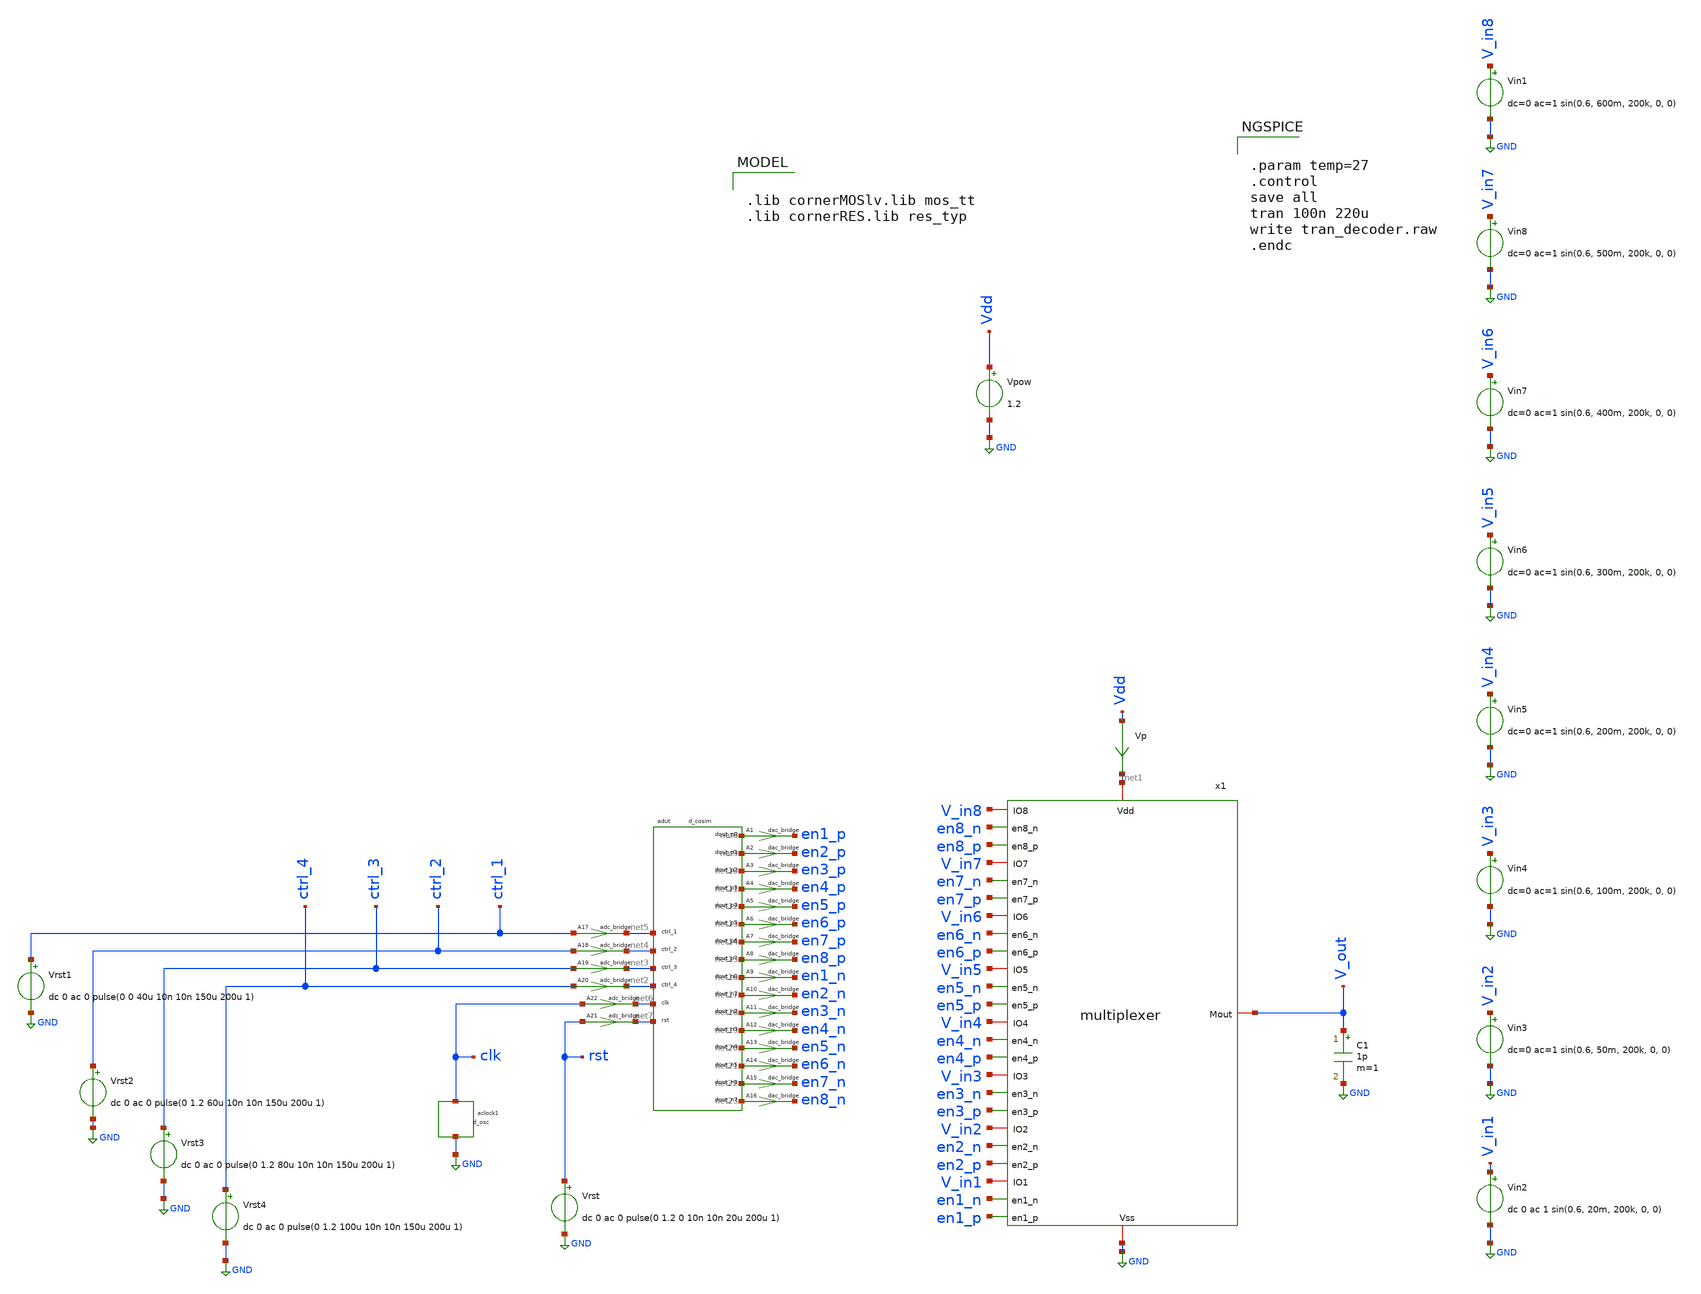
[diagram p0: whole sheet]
** sch_path: CHIPCHILE_CANELOS24_WorkshopTO/design_data/xschem/multiplexer/multiplexer_mixed_decoder_tb.sch
* Copyright 2023 IHP PDK Authors
**.subckt multiplexer_mixed_decoder_tb
Vpow Vdd GND 1.2
Vp Vdd net1 0
.save i(vp)
C1 V_out GND 1p m=1
x1 net1 V_in8 en8_n en8_p V_in7 en7_n en7_p V_in6 en6_n en6_p V_in5 en5_n en5_p V_out V_in4 en4_n
+ en4_p V_in3 en3_n en3_p V_in2 en2_n en2_p V_in1 en1_n en1_p GND multiplexer
Vin2 V_in1 GND dc 0 ac 1 sin(0.6, 20m, 200k, 0, 0)
Vin3 V_in2 GND dc=0 ac=1 sin(0.6, 50m, 200k, 0, 0)
Vin4 V_in3 GND dc=0 ac=1 sin(0.6, 100m, 200k, 0, 0)
Vin5 V_in4 GND dc=0 ac=1 sin(0.6, 200m, 200k, 0, 0)
Vin6 V_in5 GND dc=0 ac=1 sin(0.6, 300m, 200k, 0, 0)
Vin7 V_in6 GND dc=0 ac=1 sin(0.6, 400m, 200k, 0, 0)
Vin8 V_in7 GND dc=0 ac=1 sin(0.6, 500m, 200k, 0, 0)
Vin1 V_in8 GND dc=0 ac=1 sin(0.6, 600m, 200k, 0, 0)
A17 [ ctrl_1 ] [ net5 ] adc1
.model adc1 adc_bridge in_low=0.2 in_high=1.0
A18 [ ctrl_2 ] [ net4 ] adc1
.model adc1 adc_bridge in_low=0.2 in_high=1.0
A19 [ ctrl_3 ] [ net3 ] adc1
.model adc1 adc_bridge in_low=0.2 in_high=1.0
A20 [ ctrl_4 ] [ net2 ] adc1
.model adc1 adc_bridge in_low=0.2 in_high=1.0
adut [ net6 net7 net5 net4 net3 net2 ] [ net8 net9 net10 net11 net12 net13 net14 net15 net16 net17
+ net18 net19 net20 net21 net22 net23 ] null dut
.model dut d_cosim simulation=./decoder.so
Vrst rst GND dc 0 ac 0 pulse(0 1.2 0 10n 10n 20u 200u 1)
aclock1 GND clk clk
.model clk d_osc cntl_array=[-1 1] freq_array=[ 200k 200k ]
A21 [ rst ] [ net7 ] adc1
.model adc1 adc_bridge in_low=0.2 in_high=1.0
A22 [ clk ] [ net6 ] adc1
.model adc1 adc_bridge in_low=0.2 in_high=1.0
A1 [ net8 ] [ en1_p ] dac1
.model dac1 dac_bridge out_low=0.0 out_high=1.2
A2 [ net9 ] [ en2_p ] dac1
.model dac1 dac_bridge out_low=0.0 out_high=1.2
A3 [ net10 ] [ en3_p ] dac1
.model dac1 dac_bridge out_low=0.0 out_high=1.2
A4 [ net11 ] [ en4_p ] dac1
.model dac1 dac_bridge out_low=0.0 out_high=1.2
A5 [ net12 ] [ en5_p ] dac1
.model dac1 dac_bridge out_low=0.0 out_high=1.2
A6 [ net13 ] [ en6_p ] dac1
.model dac1 dac_bridge out_low=0.0 out_high=1.2
A7 [ net14 ] [ en7_p ] dac1
.model dac1 dac_bridge out_low=0.0 out_high=1.2
A8 [ net15 ] [ en8_p ] dac1
.model dac1 dac_bridge out_low=0.0 out_high=1.2
A9 [ net16 ] [ en1_n ] dac1
.model dac1 dac_bridge out_low=0.0 out_high=1.2
A10 [ net17 ] [ en2_n ] dac1
.model dac1 dac_bridge out_low=0.0 out_high=1.2
A11 [ net18 ] [ en3_n ] dac1
.model dac1 dac_bridge out_low=0.0 out_high=1.2
A12 [ net19 ] [ en4_n ] dac1
.model dac1 dac_bridge out_low=0.0 out_high=1.2
A13 [ net20 ] [ en5_n ] dac1
.model dac1 dac_bridge out_low=0.0 out_high=1.2
A14 [ net21 ] [ en6_n ] dac1
.model dac1 dac_bridge out_low=0.0 out_high=1.2
A15 [ net22 ] [ en7_n ] dac1
.model dac1 dac_bridge out_low=0.0 out_high=1.2
A16 [ net23 ] [ en8_n ] dac1
.model dac1 dac_bridge out_low=0.0 out_high=1.2
Vrst1 ctrl_1 GND dc 0 ac 0 pulse(0 0 40u 10n 10n 150u 200u 1)
Vrst2 ctrl_2 GND dc 0 ac 0 pulse(0 1.2 60u 10n 10n 150u 200u 1)
Vrst3 ctrl_3 GND dc 0 ac 0 pulse(0 1.2 80u 10n 10n 150u 200u 1)
Vrst4 ctrl_4 GND dc 0 ac 0 pulse(0 1.2 100u 10n 10n 150u 200u 1)
**** begin user architecture code

.lib cornerMOSlv.lib mos_tt
.lib cornerRES.lib res_typ



.param temp=27
.control
save all
tran 100n 220u
write tran_decoder.raw
.endc


**** end user architecture code
**.ends

* expanding   symbol:  multiplexer.sym # of pins=27
** sym_path: CHIPCHILE_CANELOS24_WorkshopTO/design_data/xschem/multiplexer/multiplexer.sym
** sch_path: CHIPCHILE_CANELOS24_WorkshopTO/design_data/xschem/multiplexer/multiplexer.sch
.subckt multiplexer Vdd IO8 en8_n en8_p IO7 en7_n en7_p IO6 en6_n en6_p IO5 en5_n en5_p Mout IO4
+ en4_n en4_p IO3 en3_n en3_p IO2 en2_n en2_p IO1 en1_n en1_p Vss
*.iopin IO1
*.iopin Vss
*.ipin en1_n
*.ipin en1_p
*.iopin IO2
*.iopin Mout
*.ipin en2_n
*.ipin en2_p
*.iopin IO3
*.ipin en3_n
*.ipin en3_p
*.iopin IO4
*.ipin en4_n
*.ipin en4_p
*.iopin IO5
*.ipin en5_n
*.ipin en5_p
*.iopin IO6
*.ipin en6_n
*.ipin en6_p
*.iopin IO7
*.ipin en7_n
*.ipin en7_p
*.iopin IO8
*.iopin Vdd
*.ipin en8_n
*.ipin en8_p
x1 Vdd en1_n IO1 Mout en1_p Vss transmission_gate
x2 Vdd en2_n IO2 Mout en2_p Vss transmission_gate
x3 Vdd en3_n IO3 Mout en3_p Vss transmission_gate
x4 Vdd en4_n IO4 Mout en4_p Vss transmission_gate
x5 Vdd en5_n IO5 Mout en5_p Vss transmission_gate
x6 Vdd en6_n IO6 Mout en6_p Vss transmission_gate
x7 Vdd en7_n IO7 Mout en7_p Vss transmission_gate
x8 Vdd en8_n IO8 Mout en8_p Vss transmission_gate
.ends


* expanding   symbol:  transmission_gate.sym # of pins=6
** sym_path: CHIPCHILE_CANELOS24_WorkshopTO/design_data/xschem/multiplexer/transmission_gate.sym
** sch_path: CHIPCHILE_CANELOS24_WorkshopTO/design_data/xschem/multiplexer/transmission_gate.sch
.subckt transmission_gate vdd en_n inout_1 inout_2 en_p vss
*.iopin inout_1
*.iopin inout_2
*.ipin en_p
*.iopin vdd
*.iopin vss
*.ipin en_n
XM1 inout_1 en_p inout_2 net1 sg13_lv_nmos w=200.0u l=0.130u ng=20 m=1 mm_ok=1
XM2 inout_1 en_n inout_2 net2 sg13_lv_pmos w=200.0u l=0.130u ng=20 m=1 mm_ok=1
XR1 vdd net2 ntap1 R=262.8 w=0.78e-6 l=0.78e-6
XR2 vss net1 ptap1 R=262.8 w=0.78e-6 l=0.78e-6
.ends

.GLOBAL GND
.end
